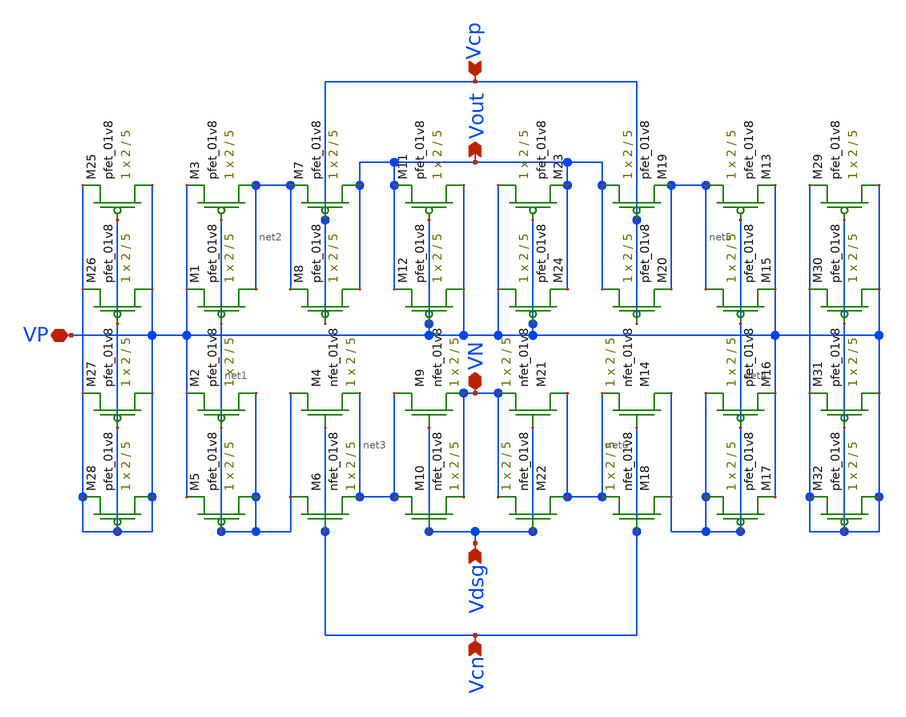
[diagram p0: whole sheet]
** sch_path: LDS_ccm_nofvf.sch
**.subckt LDS_ccm_nofvf VP Vcp Vout VN Vdsg Vcn
*.iopin VP
*.ipin Vcp
*.opin Vout
*.iopin VN
*.ipin Vdsg
*.ipin Vcn
XM3 net2 net1 VP VDD sky130_fd_pr__pfet_01v8 L=5 W=2 nf=1 ad='int((nf+1)/2) * W/nf * 0.29' as='int((nf+2)/2) * W/nf * 0.29'
+ pd='2*int((nf+1)/2) * (W/nf + 0.29)' ps='2*int((nf+2)/2) * (W/nf + 0.29)' nrd='0.29 / W' nrs='0.29 / W'
+ sa=0 sb=0 sd=0 mult=1 m=1
XM4 net1 Vcn net3 GND sky130_fd_pr__nfet_01v8 L=5 W=2 nf=1 ad='int((nf+1)/2) * W/nf * 0.29' as='int((nf+2)/2) * W/nf * 0.29'
+ pd='2*int((nf+1)/2) * (W/nf + 0.29)' ps='2*int((nf+2)/2) * (W/nf + 0.29)' nrd='0.29 / W' nrs='0.29 / W'
+ sa=0 sb=0 sd=0 mult=1 m=1
XM1 net2 net1 VP VDD sky130_fd_pr__pfet_01v8 L=5 W=2 nf=1 ad='int((nf+1)/2) * W/nf * 0.29' as='int((nf+2)/2) * W/nf * 0.29'
+ pd='2*int((nf+1)/2) * (W/nf + 0.29)' ps='2*int((nf+2)/2) * (W/nf + 0.29)' nrd='0.29 / W' nrs='0.29 / W'
+ sa=0 sb=0 sd=0 mult=1 m=1
XM2 net1 net1 VP VDD sky130_fd_pr__pfet_01v8 L=5 W=2 nf=1 ad='int((nf+1)/2) * W/nf * 0.29' as='int((nf+2)/2) * W/nf * 0.29'
+ pd='2*int((nf+1)/2) * (W/nf + 0.29)' ps='2*int((nf+2)/2) * (W/nf + 0.29)' nrd='0.29 / W' nrs='0.29 / W'
+ sa=0 sb=0 sd=0 mult=1 m=1
XM5 net1 net1 VP VDD sky130_fd_pr__pfet_01v8 L=5 W=2 nf=1 ad='int((nf+1)/2) * W/nf * 0.29' as='int((nf+2)/2) * W/nf * 0.29'
+ pd='2*int((nf+1)/2) * (W/nf + 0.29)' ps='2*int((nf+2)/2) * (W/nf + 0.29)' nrd='0.29 / W' nrs='0.29 / W'
+ sa=0 sb=0 sd=0 mult=1 m=1
XM6 net1 Vcn net3 GND sky130_fd_pr__nfet_01v8 L=5 W=2 nf=1 ad='int((nf+1)/2) * W/nf * 0.29' as='int((nf+2)/2) * W/nf * 0.29'
+ pd='2*int((nf+1)/2) * (W/nf + 0.29)' ps='2*int((nf+2)/2) * (W/nf + 0.29)' nrd='0.29 / W' nrs='0.29 / W'
+ sa=0 sb=0 sd=0 mult=1 m=1
XM7 Vout Vcp net2 VDD sky130_fd_pr__pfet_01v8 L=5 W=2 nf=1 ad='int((nf+1)/2) * W/nf * 0.29' as='int((nf+2)/2) * W/nf * 0.29'
+ pd='2*int((nf+1)/2) * (W/nf + 0.29)' ps='2*int((nf+2)/2) * (W/nf + 0.29)' nrd='0.29 / W' nrs='0.29 / W'
+ sa=0 sb=0 sd=0 mult=1 m=1
XM8 Vout Vcp net2 VDD sky130_fd_pr__pfet_01v8 L=5 W=2 nf=1 ad='int((nf+1)/2) * W/nf * 0.29' as='int((nf+2)/2) * W/nf * 0.29'
+ pd='2*int((nf+1)/2) * (W/nf + 0.29)' ps='2*int((nf+2)/2) * (W/nf + 0.29)' nrd='0.29 / W' nrs='0.29 / W'
+ sa=0 sb=0 sd=0 mult=1 m=1
XM9 net3 Vdsg VN GND sky130_fd_pr__nfet_01v8 L=5 W=2 nf=1 ad='int((nf+1)/2) * W/nf * 0.29' as='int((nf+2)/2) * W/nf * 0.29'
+ pd='2*int((nf+1)/2) * (W/nf + 0.29)' ps='2*int((nf+2)/2) * (W/nf + 0.29)' nrd='0.29 / W' nrs='0.29 / W'
+ sa=0 sb=0 sd=0 mult=1 m=1
XM10 net3 Vdsg VN GND sky130_fd_pr__nfet_01v8 L=5 W=2 nf=1 ad='int((nf+1)/2) * W/nf * 0.29' as='int((nf+2)/2) * W/nf * 0.29'
+ pd='2*int((nf+1)/2) * (W/nf + 0.29)' ps='2*int((nf+2)/2) * (W/nf + 0.29)' nrd='0.29 / W' nrs='0.29 / W'
+ sa=0 sb=0 sd=0 mult=1 m=1
XM11 VP VP Vout VDD sky130_fd_pr__pfet_01v8 L=5 W=2 nf=1 ad='int((nf+1)/2) * W/nf * 0.29' as='int((nf+2)/2) * W/nf * 0.29'
+ pd='2*int((nf+1)/2) * (W/nf + 0.29)' ps='2*int((nf+2)/2) * (W/nf + 0.29)' nrd='0.29 / W' nrs='0.29 / W'
+ sa=0 sb=0 sd=0 mult=1 m=1
XM12 VP VP Vout VDD sky130_fd_pr__pfet_01v8 L=5 W=2 nf=1 ad='int((nf+1)/2) * W/nf * 0.29' as='int((nf+2)/2) * W/nf * 0.29'
+ pd='2*int((nf+1)/2) * (W/nf + 0.29)' ps='2*int((nf+2)/2) * (W/nf + 0.29)' nrd='0.29 / W' nrs='0.29 / W'
+ sa=0 sb=0 sd=0 mult=1 m=1
XM13 net5 net4 VP VDD sky130_fd_pr__pfet_01v8 L=5 W=2 nf=1 ad='int((nf+1)/2) * W/nf * 0.29' as='int((nf+2)/2) * W/nf * 0.29'
+ pd='2*int((nf+1)/2) * (W/nf + 0.29)' ps='2*int((nf+2)/2) * (W/nf + 0.29)' nrd='0.29 / W' nrs='0.29 / W'
+ sa=0 sb=0 sd=0 mult=1 m=1
XM14 net4 Vcn net6 GND sky130_fd_pr__nfet_01v8 L=5 W=2 nf=1 ad='int((nf+1)/2) * W/nf * 0.29' as='int((nf+2)/2) * W/nf * 0.29'
+ pd='2*int((nf+1)/2) * (W/nf + 0.29)' ps='2*int((nf+2)/2) * (W/nf + 0.29)' nrd='0.29 / W' nrs='0.29 / W'
+ sa=0 sb=0 sd=0 mult=1 m=1
XM15 net5 net4 VP VDD sky130_fd_pr__pfet_01v8 L=5 W=2 nf=1 ad='int((nf+1)/2) * W/nf * 0.29' as='int((nf+2)/2) * W/nf * 0.29'
+ pd='2*int((nf+1)/2) * (W/nf + 0.29)' ps='2*int((nf+2)/2) * (W/nf + 0.29)' nrd='0.29 / W' nrs='0.29 / W'
+ sa=0 sb=0 sd=0 mult=1 m=1
XM16 net4 net4 VP VDD sky130_fd_pr__pfet_01v8 L=5 W=2 nf=1 ad='int((nf+1)/2) * W/nf * 0.29' as='int((nf+2)/2) * W/nf * 0.29'
+ pd='2*int((nf+1)/2) * (W/nf + 0.29)' ps='2*int((nf+2)/2) * (W/nf + 0.29)' nrd='0.29 / W' nrs='0.29 / W'
+ sa=0 sb=0 sd=0 mult=1 m=1
XM17 net4 net4 VP VDD sky130_fd_pr__pfet_01v8 L=5 W=2 nf=1 ad='int((nf+1)/2) * W/nf * 0.29' as='int((nf+2)/2) * W/nf * 0.29'
+ pd='2*int((nf+1)/2) * (W/nf + 0.29)' ps='2*int((nf+2)/2) * (W/nf + 0.29)' nrd='0.29 / W' nrs='0.29 / W'
+ sa=0 sb=0 sd=0 mult=1 m=1
XM18 net4 Vcn net6 GND sky130_fd_pr__nfet_01v8 L=5 W=2 nf=1 ad='int((nf+1)/2) * W/nf * 0.29' as='int((nf+2)/2) * W/nf * 0.29'
+ pd='2*int((nf+1)/2) * (W/nf + 0.29)' ps='2*int((nf+2)/2) * (W/nf + 0.29)' nrd='0.29 / W' nrs='0.29 / W'
+ sa=0 sb=0 sd=0 mult=1 m=1
XM19 Vout Vcp net5 VDD sky130_fd_pr__pfet_01v8 L=5 W=2 nf=1 ad='int((nf+1)/2) * W/nf * 0.29' as='int((nf+2)/2) * W/nf * 0.29'
+ pd='2*int((nf+1)/2) * (W/nf + 0.29)' ps='2*int((nf+2)/2) * (W/nf + 0.29)' nrd='0.29 / W' nrs='0.29 / W'
+ sa=0 sb=0 sd=0 mult=1 m=1
XM20 Vout Vcp net5 VDD sky130_fd_pr__pfet_01v8 L=5 W=2 nf=1 ad='int((nf+1)/2) * W/nf * 0.29' as='int((nf+2)/2) * W/nf * 0.29'
+ pd='2*int((nf+1)/2) * (W/nf + 0.29)' ps='2*int((nf+2)/2) * (W/nf + 0.29)' nrd='0.29 / W' nrs='0.29 / W'
+ sa=0 sb=0 sd=0 mult=1 m=1
XM21 net6 Vdsg VN GND sky130_fd_pr__nfet_01v8 L=5 W=2 nf=1 ad='int((nf+1)/2) * W/nf * 0.29' as='int((nf+2)/2) * W/nf * 0.29'
+ pd='2*int((nf+1)/2) * (W/nf + 0.29)' ps='2*int((nf+2)/2) * (W/nf + 0.29)' nrd='0.29 / W' nrs='0.29 / W'
+ sa=0 sb=0 sd=0 mult=1 m=1
XM22 net6 Vdsg VN GND sky130_fd_pr__nfet_01v8 L=5 W=2 nf=1 ad='int((nf+1)/2) * W/nf * 0.29' as='int((nf+2)/2) * W/nf * 0.29'
+ pd='2*int((nf+1)/2) * (W/nf + 0.29)' ps='2*int((nf+2)/2) * (W/nf + 0.29)' nrd='0.29 / W' nrs='0.29 / W'
+ sa=0 sb=0 sd=0 mult=1 m=1
XM23 VP VP Vout VDD sky130_fd_pr__pfet_01v8 L=5 W=2 nf=1 ad='int((nf+1)/2) * W/nf * 0.29' as='int((nf+2)/2) * W/nf * 0.29'
+ pd='2*int((nf+1)/2) * (W/nf + 0.29)' ps='2*int((nf+2)/2) * (W/nf + 0.29)' nrd='0.29 / W' nrs='0.29 / W'
+ sa=0 sb=0 sd=0 mult=1 m=1
XM24 VP VP Vout VDD sky130_fd_pr__pfet_01v8 L=5 W=2 nf=1 ad='int((nf+1)/2) * W/nf * 0.29' as='int((nf+2)/2) * W/nf * 0.29'
+ pd='2*int((nf+1)/2) * (W/nf + 0.29)' ps='2*int((nf+2)/2) * (W/nf + 0.29)' nrd='0.29 / W' nrs='0.29 / W'
+ sa=0 sb=0 sd=0 mult=1 m=1
XM25 VP VP VP VDD sky130_fd_pr__pfet_01v8 L=5 W=2 nf=1 ad='int((nf+1)/2) * W/nf * 0.29' as='int((nf+2)/2) * W/nf * 0.29'
+ pd='2*int((nf+1)/2) * (W/nf + 0.29)' ps='2*int((nf+2)/2) * (W/nf + 0.29)' nrd='0.29 / W' nrs='0.29 / W'
+ sa=0 sb=0 sd=0 mult=1 m=1
XM26 VP VP VP VDD sky130_fd_pr__pfet_01v8 L=5 W=2 nf=1 ad='int((nf+1)/2) * W/nf * 0.29' as='int((nf+2)/2) * W/nf * 0.29'
+ pd='2*int((nf+1)/2) * (W/nf + 0.29)' ps='2*int((nf+2)/2) * (W/nf + 0.29)' nrd='0.29 / W' nrs='0.29 / W'
+ sa=0 sb=0 sd=0 mult=1 m=1
XM27 VP VP VP VDD sky130_fd_pr__pfet_01v8 L=5 W=2 nf=1 ad='int((nf+1)/2) * W/nf * 0.29' as='int((nf+2)/2) * W/nf * 0.29'
+ pd='2*int((nf+1)/2) * (W/nf + 0.29)' ps='2*int((nf+2)/2) * (W/nf + 0.29)' nrd='0.29 / W' nrs='0.29 / W'
+ sa=0 sb=0 sd=0 mult=1 m=1
XM28 VP VP VP VDD sky130_fd_pr__pfet_01v8 L=5 W=2 nf=1 ad='int((nf+1)/2) * W/nf * 0.29' as='int((nf+2)/2) * W/nf * 0.29'
+ pd='2*int((nf+1)/2) * (W/nf + 0.29)' ps='2*int((nf+2)/2) * (W/nf + 0.29)' nrd='0.29 / W' nrs='0.29 / W'
+ sa=0 sb=0 sd=0 mult=1 m=1
XM29 VP VP VP VDD sky130_fd_pr__pfet_01v8 L=5 W=2 nf=1 ad='int((nf+1)/2) * W/nf * 0.29' as='int((nf+2)/2) * W/nf * 0.29'
+ pd='2*int((nf+1)/2) * (W/nf + 0.29)' ps='2*int((nf+2)/2) * (W/nf + 0.29)' nrd='0.29 / W' nrs='0.29 / W'
+ sa=0 sb=0 sd=0 mult=1 m=1
XM30 VP VP VP VDD sky130_fd_pr__pfet_01v8 L=5 W=2 nf=1 ad='int((nf+1)/2) * W/nf * 0.29' as='int((nf+2)/2) * W/nf * 0.29'
+ pd='2*int((nf+1)/2) * (W/nf + 0.29)' ps='2*int((nf+2)/2) * (W/nf + 0.29)' nrd='0.29 / W' nrs='0.29 / W'
+ sa=0 sb=0 sd=0 mult=1 m=1
XM31 VP VP VP VDD sky130_fd_pr__pfet_01v8 L=5 W=2 nf=1 ad='int((nf+1)/2) * W/nf * 0.29' as='int((nf+2)/2) * W/nf * 0.29'
+ pd='2*int((nf+1)/2) * (W/nf + 0.29)' ps='2*int((nf+2)/2) * (W/nf + 0.29)' nrd='0.29 / W' nrs='0.29 / W'
+ sa=0 sb=0 sd=0 mult=1 m=1
XM32 VP VP VP VDD sky130_fd_pr__pfet_01v8 L=5 W=2 nf=1 ad='int((nf+1)/2) * W/nf * 0.29' as='int((nf+2)/2) * W/nf * 0.29'
+ pd='2*int((nf+1)/2) * (W/nf + 0.29)' ps='2*int((nf+2)/2) * (W/nf + 0.29)' nrd='0.29 / W' nrs='0.29 / W'
+ sa=0 sb=0 sd=0 mult=1 m=1
**.ends
.end
